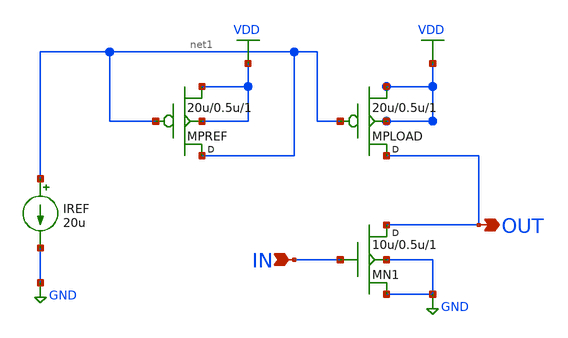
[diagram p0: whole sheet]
** sch_path: E3_238_Analog_VLSI_Circuits/08_Current_Source_Load_CS_Amplifier/cs_current_source_load.sch
**.subckt cs_current_source_load IN OUT
*.ipin IN
*.opin OUT
MPREF net1 net1 VDD VDD pmos w=20u l=0.5u m=1
MPLOAD OUT net1 VDD VDD pmos w=20u l=0.5u m=1
MN1 OUT IN GND GND nmos w=10u l=0.5u m=1
IREF net1 GND 20u
**** begin user architecture code

.include /home/anirudh/Analog_VLSI_Projects/models/cmos_180nm.mod
VDD VDD 0 DC 1.8
VIN IN 0 DC 0.55 AC 1
CL OUT GND 1p

.control
  dc VIN 0.5 0.65 0.01
  plot v(OUT) vs v(IN)
  alter VIN dc=0.55
  op
  print v(OUT)
  ac dec 20 1 1G
  plot db(v(OUT))
  plot phase(v(OUT))*180/pi
.endc


**** end user architecture code
**.ends
.GLOBAL VDD
.GLOBAL GND
.end
